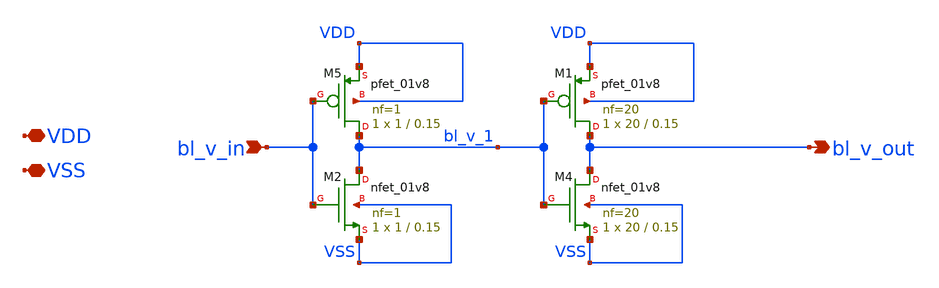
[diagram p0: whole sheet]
** sch_path: xschem/bl_inverter.sch
**.subckt bl_inverter VDD VSS bl_v_in bl_v_out
*.iopin VDD
*.iopin VSS
*.ipin bl_v_in
*.opin bl_v_out
XM2 bl_v_1 bl_v_in VSS VSS sky130_fd_pr__nfet_01v8 L=0.15 W=1 nf=1 ad='int((nf+1)/2) * W/nf * 0.29' as='int((nf+2)/2) * W/nf * 0.29'
+ pd='2*int((nf+1)/2) * (W/nf + 0.29)' ps='2*int((nf+2)/2) * (W/nf + 0.29)' nrd='0.29 / W' nrs='0.29 / W'
+ sa=0 sb=0 sd=0 mult=1 m=1
XM4 bl_v_out bl_v_1 VSS VSS sky130_fd_pr__nfet_01v8 L=0.15 W=20 nf=20 ad='int((nf+1)/2) * W/nf * 0.29'
+ as='int((nf+2)/2) * W/nf * 0.29' pd='2*int((nf+1)/2) * (W/nf + 0.29)' ps='2*int((nf+2)/2) * (W/nf + 0.29)'
+ nrd='0.29 / W' nrs='0.29 / W' sa=0 sb=0 sd=0 mult=1 m=1
XM5 bl_v_1 bl_v_in VDD VDD sky130_fd_pr__pfet_01v8 L=0.15 W=1 nf=1 ad='int((nf+1)/2) * W/nf * 0.29' as='int((nf+2)/2) * W/nf * 0.29'
+ pd='2*int((nf+1)/2) * (W/nf + 0.29)' ps='2*int((nf+2)/2) * (W/nf + 0.29)' nrd='0.29 / W' nrs='0.29 / W'
+ sa=0 sb=0 sd=0 mult=1 m=1
XM1 bl_v_out bl_v_1 VDD VDD sky130_fd_pr__pfet_01v8 L=0.15 W=20 nf=20 ad='int((nf+1)/2) * W/nf * 0.29'
+ as='int((nf+2)/2) * W/nf * 0.29' pd='2*int((nf+1)/2) * (W/nf + 0.29)' ps='2*int((nf+2)/2) * (W/nf + 0.29)'
+ nrd='0.29 / W' nrs='0.29 / W' sa=0 sb=0 sd=0 mult=1 m=1
**.ends
.end
